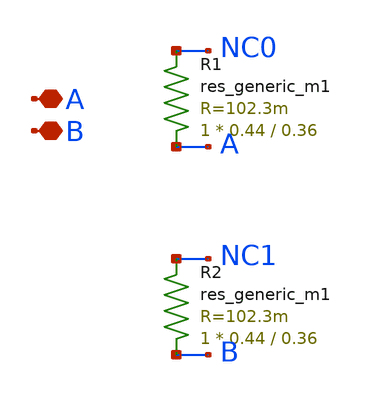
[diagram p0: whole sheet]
** sch_path: ip/sun_sar9b_sky130nm/design/SUN_SAR9B_SKY130NM/SUNSAR_CAP_BSSW_CV.sch
**.subckt SUNSAR_CAP_BSSW_CV A B
*.iopin A
*.iopin B
R1 A NC0 sky130_fd_pr__res_generic_m1 W=0.44 L=0.36 m=1
R2 B NC1 sky130_fd_pr__res_generic_m1 W=0.44 L=0.36 m=1
**.ends
.end
